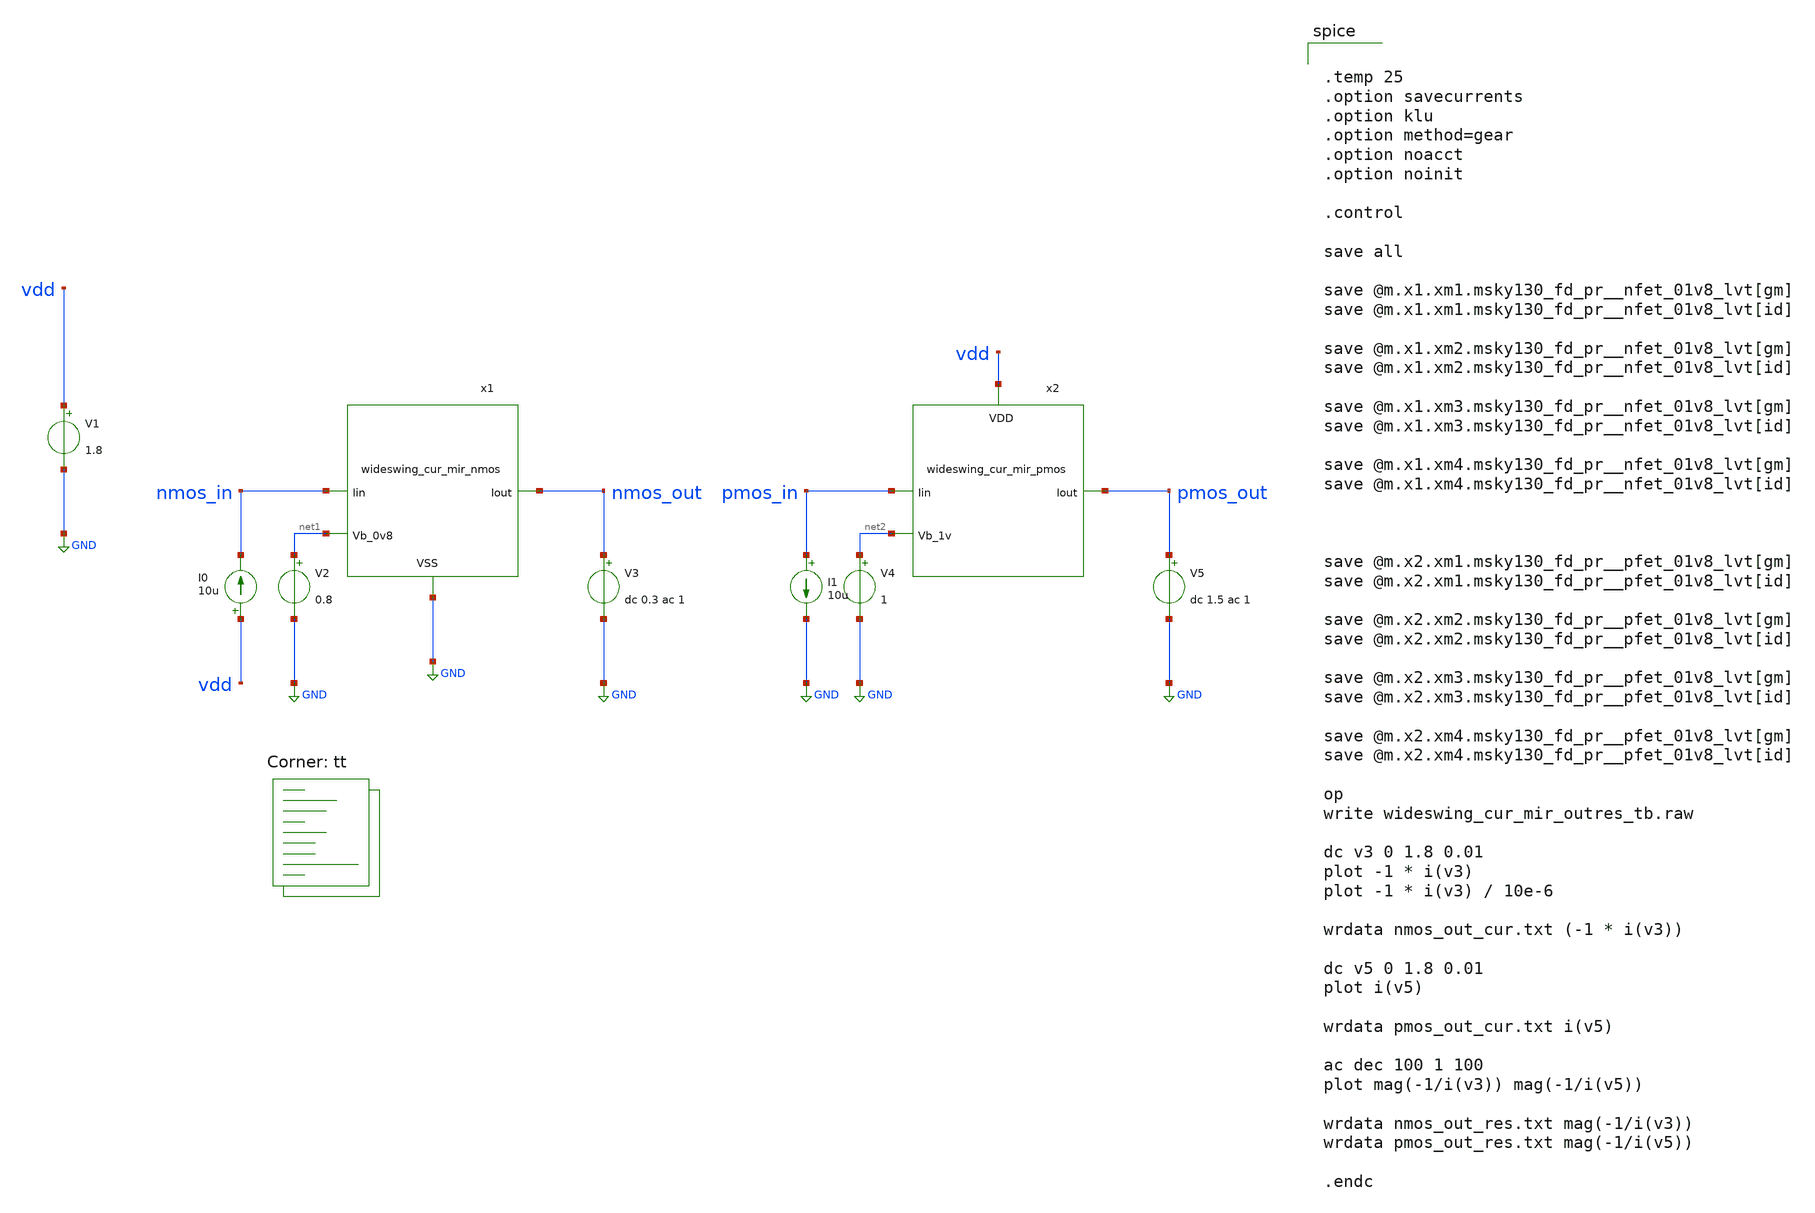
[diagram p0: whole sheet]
** sch_path: xschem/wideswing_cur_mir_outres_tb.sch
**.subckt wideswing_cur_mir_outres_tb
V1 vdd GND 1.8
.save i(v1)
x1 GND net1 nmos_in nmos_out wideswing_cur_mir_nmos
V2 net1 GND 0.8
.save i(v2)
I0 vdd nmos_in 10u
V3 nmos_out GND dc 0.3 ac 1
.save i(v3)
x2 vdd net2 pmos_in pmos_out wideswing_cur_mir_pmos
V4 net2 GND 1
.save i(v4)
I1 pmos_in GND 10u
V5 pmos_out GND dc 1.5 ac 1
.save i(v5)
**** begin user architecture code
.lib $::SKYWATER_MODELS/sky130.lib.spice tt


.temp 25
.option savecurrents
.option klu
.option method=gear
.option noacct
.option noinit

.control

save all

save @m.x1.xm1.msky130_fd_pr__nfet_01v8_lvt[gm]
save @m.x1.xm1.msky130_fd_pr__nfet_01v8_lvt[id]

save @m.x1.xm2.msky130_fd_pr__nfet_01v8_lvt[gm]
save @m.x1.xm2.msky130_fd_pr__nfet_01v8_lvt[id]

save @m.x1.xm3.msky130_fd_pr__nfet_01v8_lvt[gm]
save @m.x1.xm3.msky130_fd_pr__nfet_01v8_lvt[id]

save @m.x1.xm4.msky130_fd_pr__nfet_01v8_lvt[gm]
save @m.x1.xm4.msky130_fd_pr__nfet_01v8_lvt[id]



save @m.x2.xm1.msky130_fd_pr__pfet_01v8_lvt[gm]
save @m.x2.xm1.msky130_fd_pr__pfet_01v8_lvt[id]

save @m.x2.xm2.msky130_fd_pr__pfet_01v8_lvt[gm]
save @m.x2.xm2.msky130_fd_pr__pfet_01v8_lvt[id]

save @m.x2.xm3.msky130_fd_pr__pfet_01v8_lvt[gm]
save @m.x2.xm3.msky130_fd_pr__pfet_01v8_lvt[id]

save @m.x2.xm4.msky130_fd_pr__pfet_01v8_lvt[gm]
save @m.x2.xm4.msky130_fd_pr__pfet_01v8_lvt[id]

op
write wideswing_cur_mir_outres_tb.raw

dc v3 0 1.8 0.01
plot -1 * i(v3)
plot -1 * i(v3) / 10e-6

wrdata nmos_out_cur.txt (-1 * i(v3))

dc v5 0 1.8 0.01
plot i(v5)

wrdata pmos_out_cur.txt i(v5)

ac dec 100 1 100
plot mag(-1/i(v3)) mag(-1/i(v5))

wrdata nmos_out_res.txt mag(-1/i(v3))
wrdata pmos_out_res.txt mag(-1/i(v5))

.endc

**** end user architecture code
**.ends

* expanding   symbol:  wideswing_cur_mir_nmos.sym # of pins=4
** sym_path: xschem/wideswing_cur_mir_nmos.sym
** sch_path: xschem/wideswing_cur_mir_nmos.sch
.subckt wideswing_cur_mir_nmos VSS Vb_0v8 Iin Iout
*.ipin Iin
*.opin Iout
*.ipin Vb_0v8
*.iopin VSS
XM1 net1 Iin VSS VSS sky130_fd_pr__nfet_01v8_lvt L=8 W=100 nf=1 ad='int((1 + 1)/2) * 100 / 1 * 0.29'
+ as='int((1 + 2)/2) * 100 / 1 * 0.29' pd='2*int((1 + 1)/2) * (100 / 1 + 0.29)' ps='2*int((1 + 2)/2) * (100 / 1 + 0.29)'
+ nrd='0.29 / 100 ' nrs='0.29 / 100 ' sa=0 sb=0 sd=0 mult=1 m=1
XM2 net2 Iin VSS VSS sky130_fd_pr__nfet_01v8_lvt L=8 W=100 nf=1 ad='int((1 + 1)/2) * 100 / 1 * 0.29'
+ as='int((1 + 2)/2) * 100 / 1 * 0.29' pd='2*int((1 + 1)/2) * (100 / 1 + 0.29)' ps='2*int((1 + 2)/2) * (100 / 1 + 0.29)'
+ nrd='0.29 / 100 ' nrs='0.29 / 100 ' sa=0 sb=0 sd=0 mult=1 m=1
XM3 Iin Vb_0v8 net1 VSS sky130_fd_pr__nfet_01v8_lvt L=8 W=100 nf=1 ad='int((1 + 1)/2) * 100 / 1 * 0.29'
+ as='int((1 + 2)/2) * 100 / 1 * 0.29' pd='2*int((1 + 1)/2) * (100 / 1 + 0.29)' ps='2*int((1 + 2)/2) * (100 / 1 + 0.29)'
+ nrd='0.29 / 100 ' nrs='0.29 / 100 ' sa=0 sb=0 sd=0 mult=1 m=1
XM4 Iout Vb_0v8 net2 VSS sky130_fd_pr__nfet_01v8_lvt L=8 W=100 nf=1 ad='int((1 + 1)/2) * 100 / 1 * 0.29'
+ as='int((1 + 2)/2) * 100 / 1 * 0.29' pd='2*int((1 + 1)/2) * (100 / 1 + 0.29)' ps='2*int((1 + 2)/2) * (100 / 1 + 0.29)'
+ nrd='0.29 / 100 ' nrs='0.29 / 100 ' sa=0 sb=0 sd=0 mult=1 m=1
.ends


* expanding   symbol:  wideswing_cur_mir_pmos.sym # of pins=4
** sym_path: xschem/wideswing_cur_mir_pmos.sym
** sch_path: xschem/wideswing_cur_mir_pmos.sch
.subckt wideswing_cur_mir_pmos VDD Vb_1v Iin Iout
*.opin Iout
*.ipin Iin
*.ipin Vb_1v
*.iopin VDD
XM1 net1 Iin VDD VDD sky130_fd_pr__pfet_01v8_lvt L=8 W=200 nf=1 ad='int((1 + 1)/2) * 200 / 1 * 0.29'
+ as='int((1 + 2)/2) * 200 / 1 * 0.29' pd='2*int((1 + 1)/2) * (200 / 1 + 0.29)' ps='2*int((1 + 2)/2) * (200 / 1 + 0.29)'
+ nrd='0.29 / 200 ' nrs='0.29 / 200 ' sa=0 sb=0 sd=0 mult=2 m=2
XM2 Iin Vb_1v net1 VDD sky130_fd_pr__pfet_01v8_lvt L=8 W=200 nf=1 ad='int((1 + 1)/2) * 200 / 1 * 0.29'
+ as='int((1 + 2)/2) * 200 / 1 * 0.29' pd='2*int((1 + 1)/2) * (200 / 1 + 0.29)' ps='2*int((1 + 2)/2) * (200 / 1 + 0.29)'
+ nrd='0.29 / 200 ' nrs='0.29 / 200 ' sa=0 sb=0 sd=0 mult=2 m=2
XM3 net2 Iin VDD VDD sky130_fd_pr__pfet_01v8_lvt L=8 W=200 nf=1 ad='int((1 + 1)/2) * 200 / 1 * 0.29'
+ as='int((1 + 2)/2) * 200 / 1 * 0.29' pd='2*int((1 + 1)/2) * (200 / 1 + 0.29)' ps='2*int((1 + 2)/2) * (200 / 1 + 0.29)'
+ nrd='0.29 / 200 ' nrs='0.29 / 200 ' sa=0 sb=0 sd=0 mult=2 m=2
XM4 Iout Vb_1v net2 VDD sky130_fd_pr__pfet_01v8_lvt L=8 W=200 nf=1 ad='int((1 + 1)/2) * 200 / 1 * 0.29'
+ as='int((1 + 2)/2) * 200 / 1 * 0.29' pd='2*int((1 + 1)/2) * (200 / 1 + 0.29)' ps='2*int((1 + 2)/2) * (200 / 1 + 0.29)'
+ nrd='0.29 / 200 ' nrs='0.29 / 200 ' sa=0 sb=0 sd=0 mult=2 m=2
.ends

.GLOBAL GND
.end
